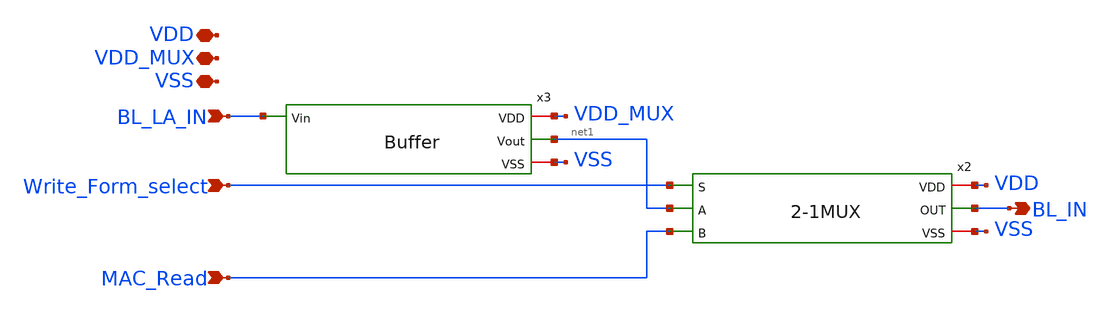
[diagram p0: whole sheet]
** sch_path: xschem/1LineBitInput.sch
**.subckt 1LineBitInput BL_LA_IN Write_Form_select MAC_Read VDD VDD_MUX VSS BL_IN
*.ipin BL_LA_IN
*.ipin Write_Form_select
*.ipin MAC_Read
*.iopin VDD
*.iopin VDD_MUX
*.iopin VSS
*.opin BL_IN
x2 VDD Write_Form_select net1 BL_IN MAC_Read VSS 2-1MUX
x3 VDD_MUX BL_LA_IN net1 VSS Buffer
**.ends

* expanding   symbol:  2-1MUX.sym # of pins=6
** sym_path: xschem/2-1MUX.sym
** sch_path: xschem/2-1MUX.sch
.subckt 2-1MUX VDD S A OUT B VSS
*.ipin A
*.ipin B
*.ipin S
*.iopin VDD
*.iopin VSS
*.opin OUT
x1 net1 VDD OUT A VSS S TransmissionGate
x2 S VDD OUT B VSS net1 TransmissionGate
x3 VDD S net1 VSS Inverter
.ends


* expanding   symbol:  Buffer.sym # of pins=4
** sym_path: xschem/Buffer.sym
** sch_path: xschem/Buffer.sch
.subckt Buffer VDD Vin Vout VSS
*.iopin VDD
*.iopin VSS
*.ipin Vin
*.opin Vout
x1 VDD Vin net1 VSS Inverter
x2 VDD net1 Vout VSS Inverter
.ends


* expanding   symbol:  TransmissionGate.sym # of pins=6
** sym_path: xschem/TransmissionGate.sym
** sch_path: xschem/TransmissionGate.sch
.subckt TransmissionGate SP VDD Out In VSS SN
*.opin Out
*.ipin In
*.ipin SP
*.iopin VDD
*.iopin VSS
*.ipin SN
XM1 In SN Out VSS sky130_fd_pr__nfet_g5v0d10v5 L=0.5 W=0.75 nf=1 ad='int((nf+1)/2) * W/nf * 0.29' as='int((nf+2)/2) * W/nf * 0.29'
+ pd='2*int((nf+1)/2) * (W/nf + 0.29)' ps='2*int((nf+2)/2) * (W/nf + 0.29)' nrd='0.29 / W' nrs='0.29 / W'
+ sa=0 sb=0 sd=0 mult=1 m=1
XM2 In SP Out VDD sky130_fd_pr__pfet_g5v0d10v5 L=0.5 W=1.5 nf=1 ad='int((nf+1)/2) * W/nf * 0.29' as='int((nf+2)/2) * W/nf * 0.29'
+ pd='2*int((nf+1)/2) * (W/nf + 0.29)' ps='2*int((nf+2)/2) * (W/nf + 0.29)' nrd='0.29 / W' nrs='0.29 / W'
+ sa=0 sb=0 sd=0 mult=1 m=1
.ends


* expanding   symbol:  Inverter.sym # of pins=4
** sym_path: xschem/Inverter.sym
** sch_path: xschem/Inverter.sch
.subckt Inverter VDD Vin Vout VSS
*.ipin Vin
*.iopin VDD
*.iopin VSS
*.opin Vout
XM1 Vout Vin VSS VSS sky130_fd_pr__nfet_g5v0d10v5 L=0.5 W=0.75 nf=1 ad='int((nf+1)/2) * W/nf * 0.29'
+ as='int((nf+2)/2) * W/nf * 0.29' pd='2*int((nf+1)/2) * (W/nf + 0.29)' ps='2*int((nf+2)/2) * (W/nf + 0.29)'
+ nrd='0.29 / W' nrs='0.29 / W' sa=0 sb=0 sd=0 mult=1 m=1
XM2 Vout Vin VDD VDD sky130_fd_pr__pfet_g5v0d10v5 L=0.5 W=1.5 nf=1 ad='int((nf+1)/2) * W/nf * 0.29' as='int((nf+2)/2) * W/nf * 0.29'
+ pd='2*int((nf+1)/2) * (W/nf + 0.29)' ps='2*int((nf+2)/2) * (W/nf + 0.29)' nrd='0.29 / W' nrs='0.29 / W'
+ sa=0 sb=0 sd=0 mult=1 m=1
.ends

.end
